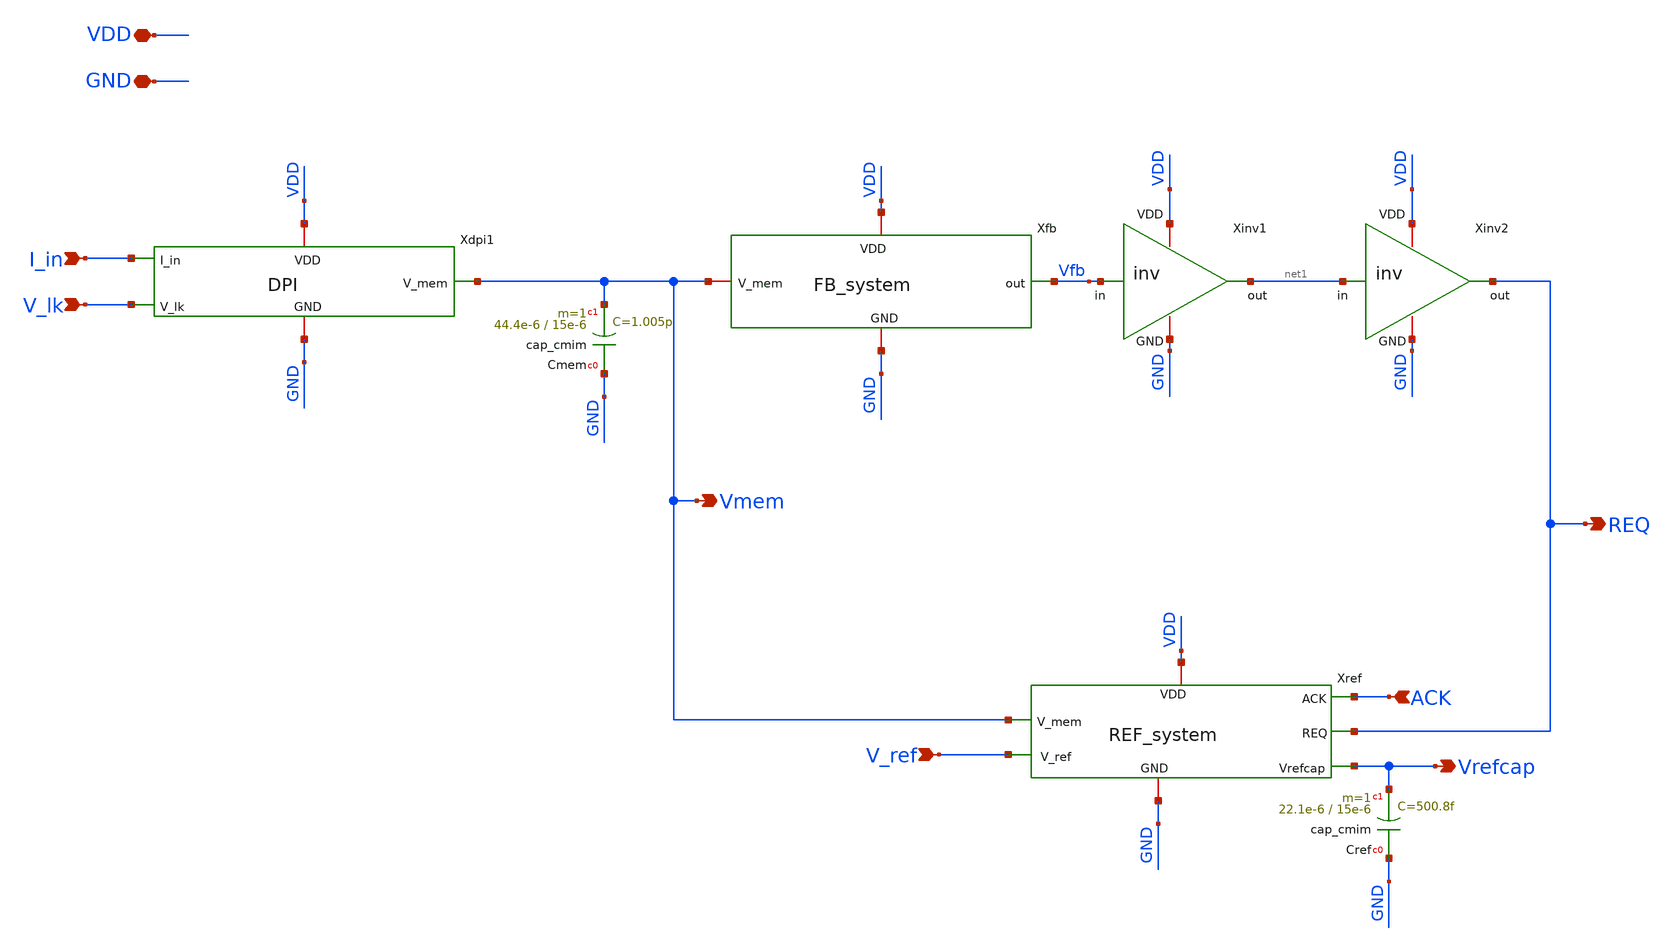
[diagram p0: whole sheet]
** sch_path: xschem/neuron_noahp.sch
**.subckt neuron_noahp V_ref GND VDD REQ ACK I_in V_lk Vmem Vrefcap
*.ipin V_ref
*.iopin GND
*.iopin VDD
*.opin REQ
*.ipin ACK
*.ipin I_in
*.ipin V_lk
*.opin Vmem
*.opin Vrefcap
Xinv1 VDD net1 Vfb GND inv
Xinv2 VDD REQ net1 GND inv
Xdpi1 I_in VDD Vmem V_lk GND DPI
Xfb VDD Vfb Vmem GND FB_system
Xref ACK Vmem REQ Vrefcap GND V_ref VDD REF_system
XCmem GND Vmem cap_cmim w=44.4e-6 l=15e-6 m=1 mm_ok=1
XCref GND Vrefcap cap_cmim w=22.1e-6 l=15e-6 m=1 mm_ok=1
**.ends
.end
